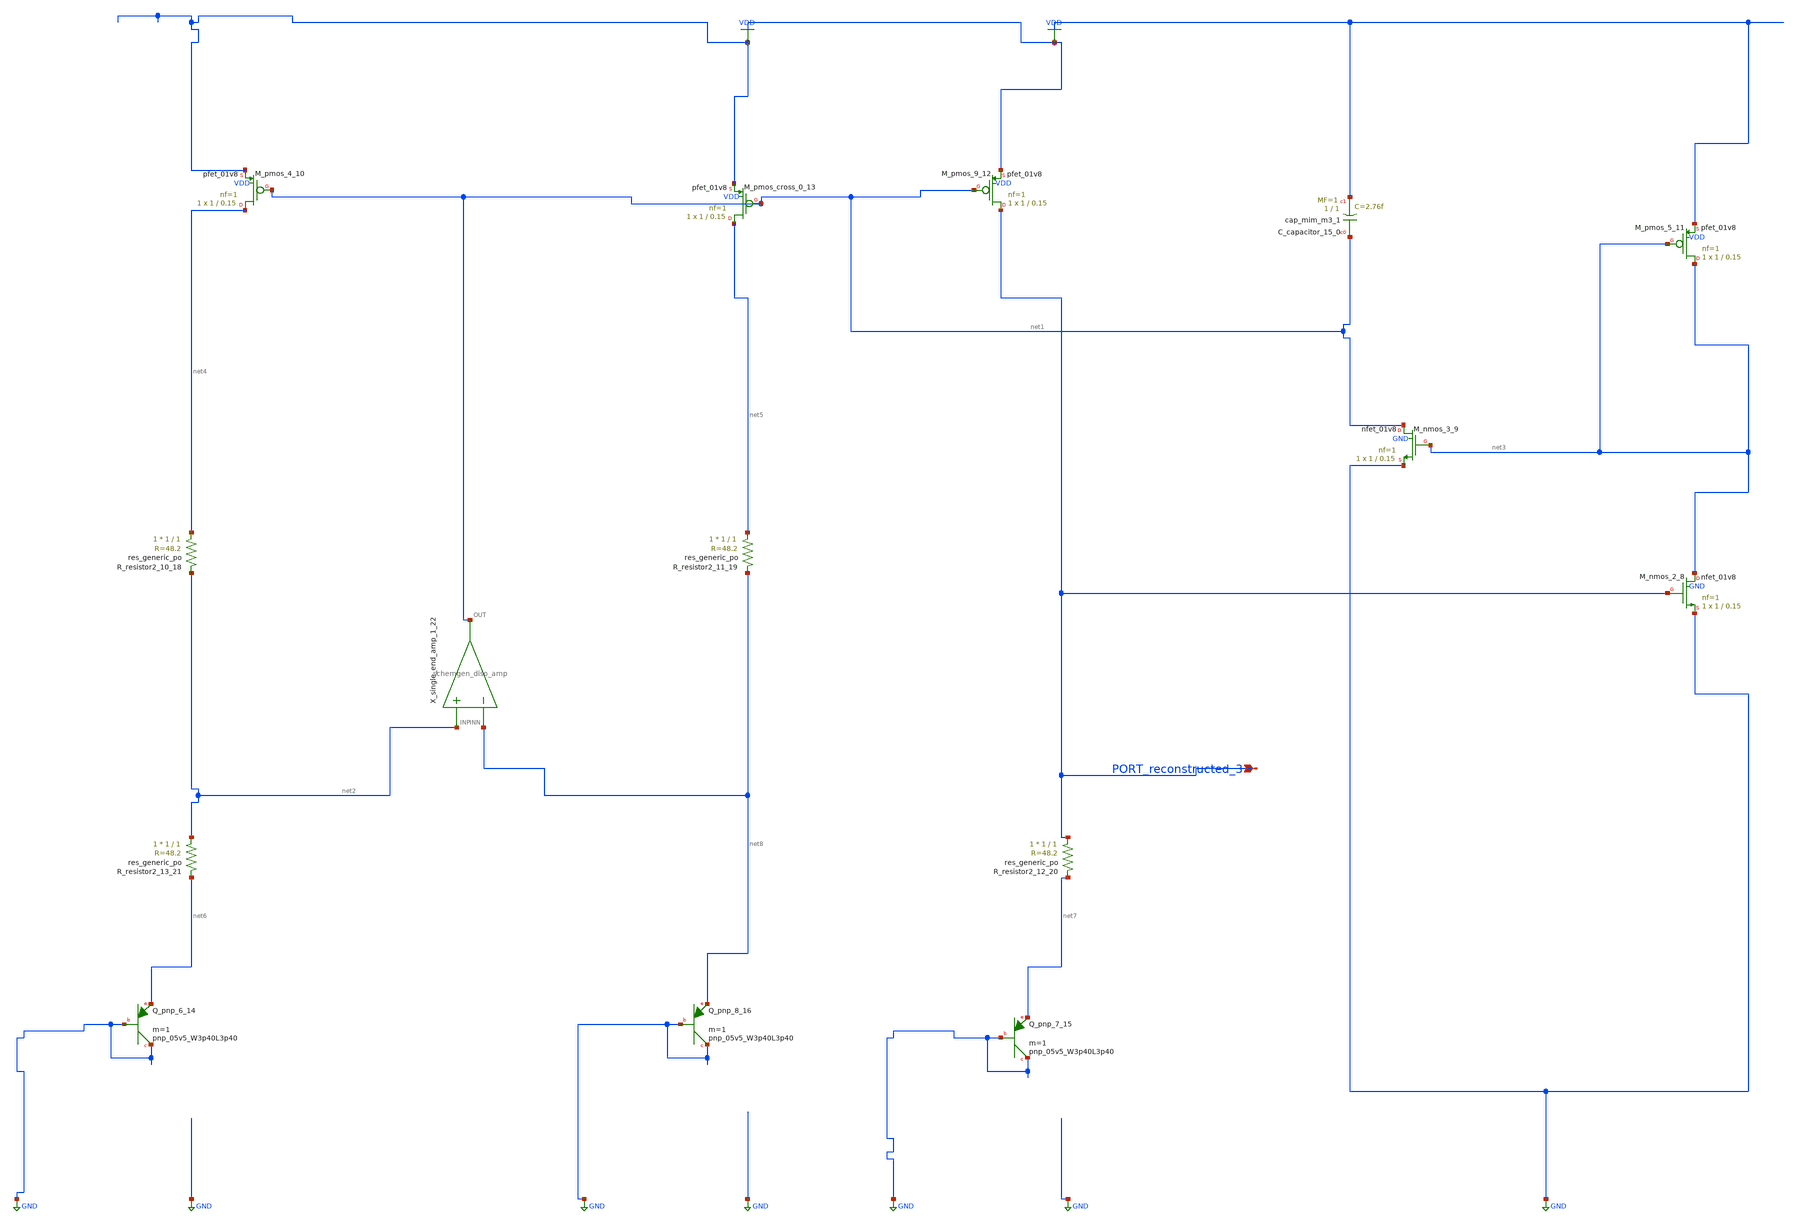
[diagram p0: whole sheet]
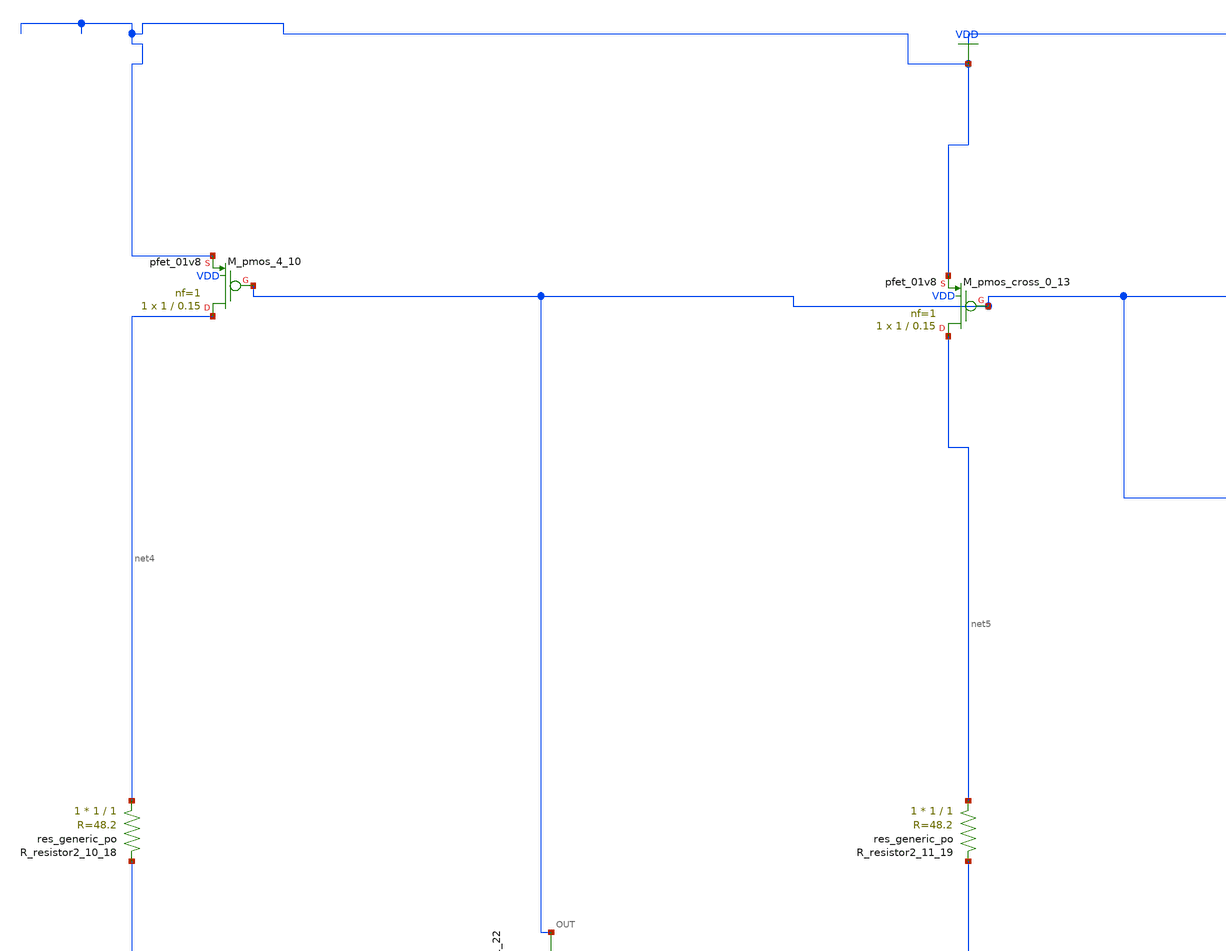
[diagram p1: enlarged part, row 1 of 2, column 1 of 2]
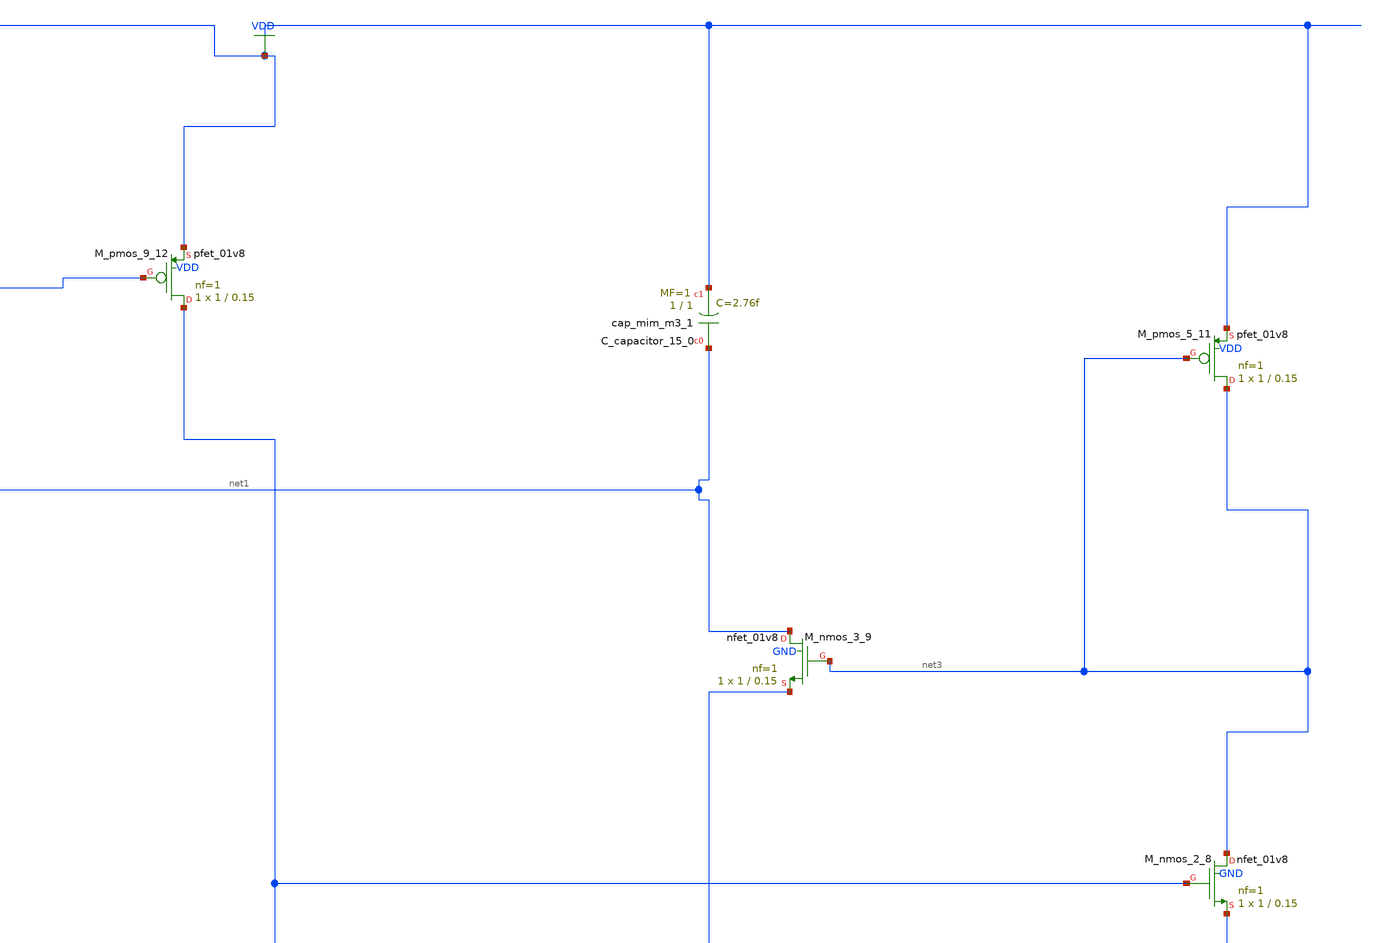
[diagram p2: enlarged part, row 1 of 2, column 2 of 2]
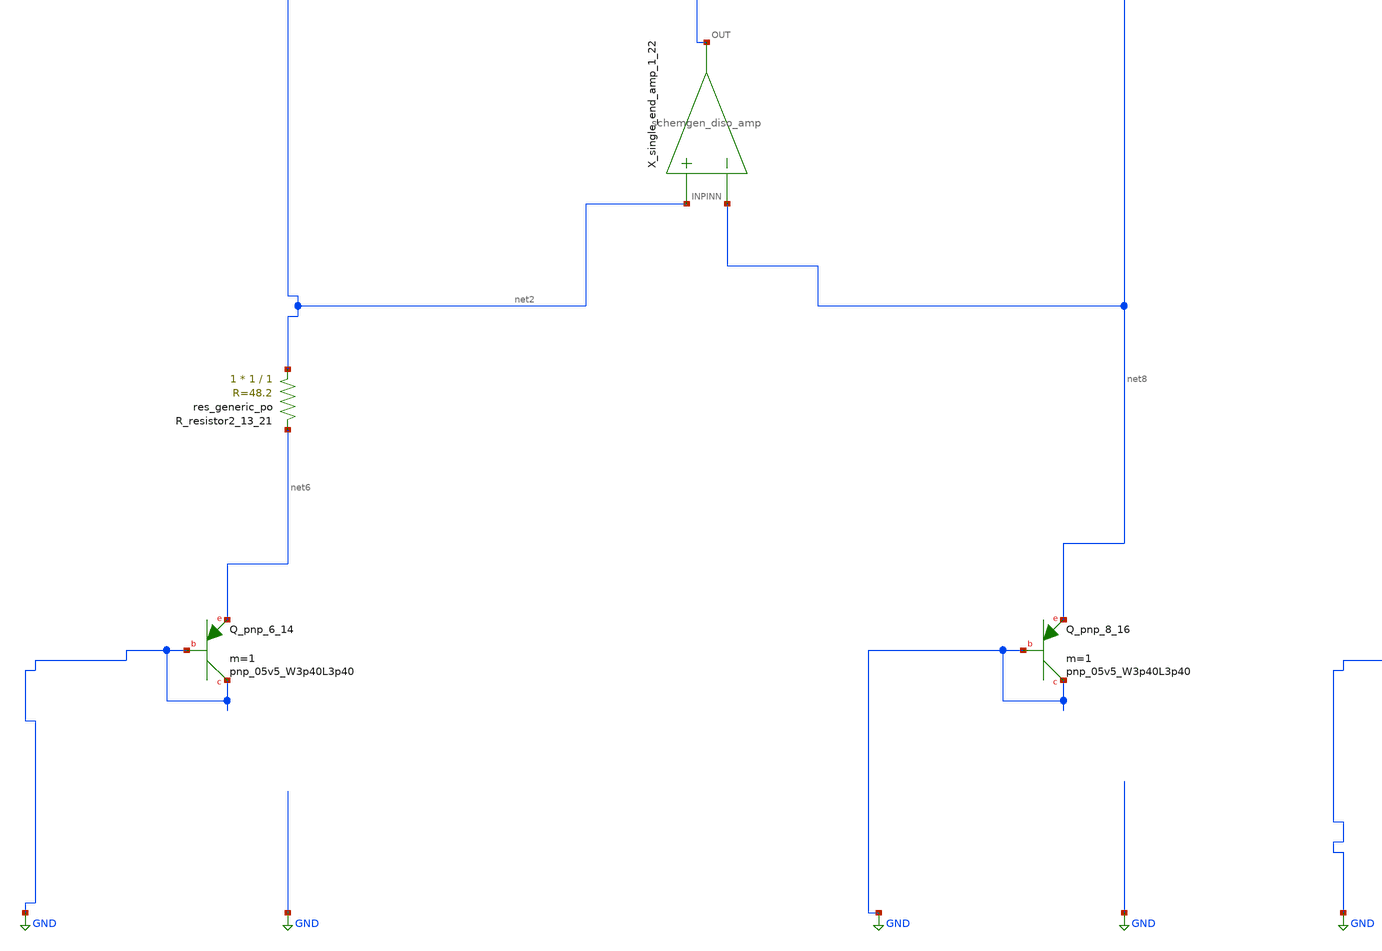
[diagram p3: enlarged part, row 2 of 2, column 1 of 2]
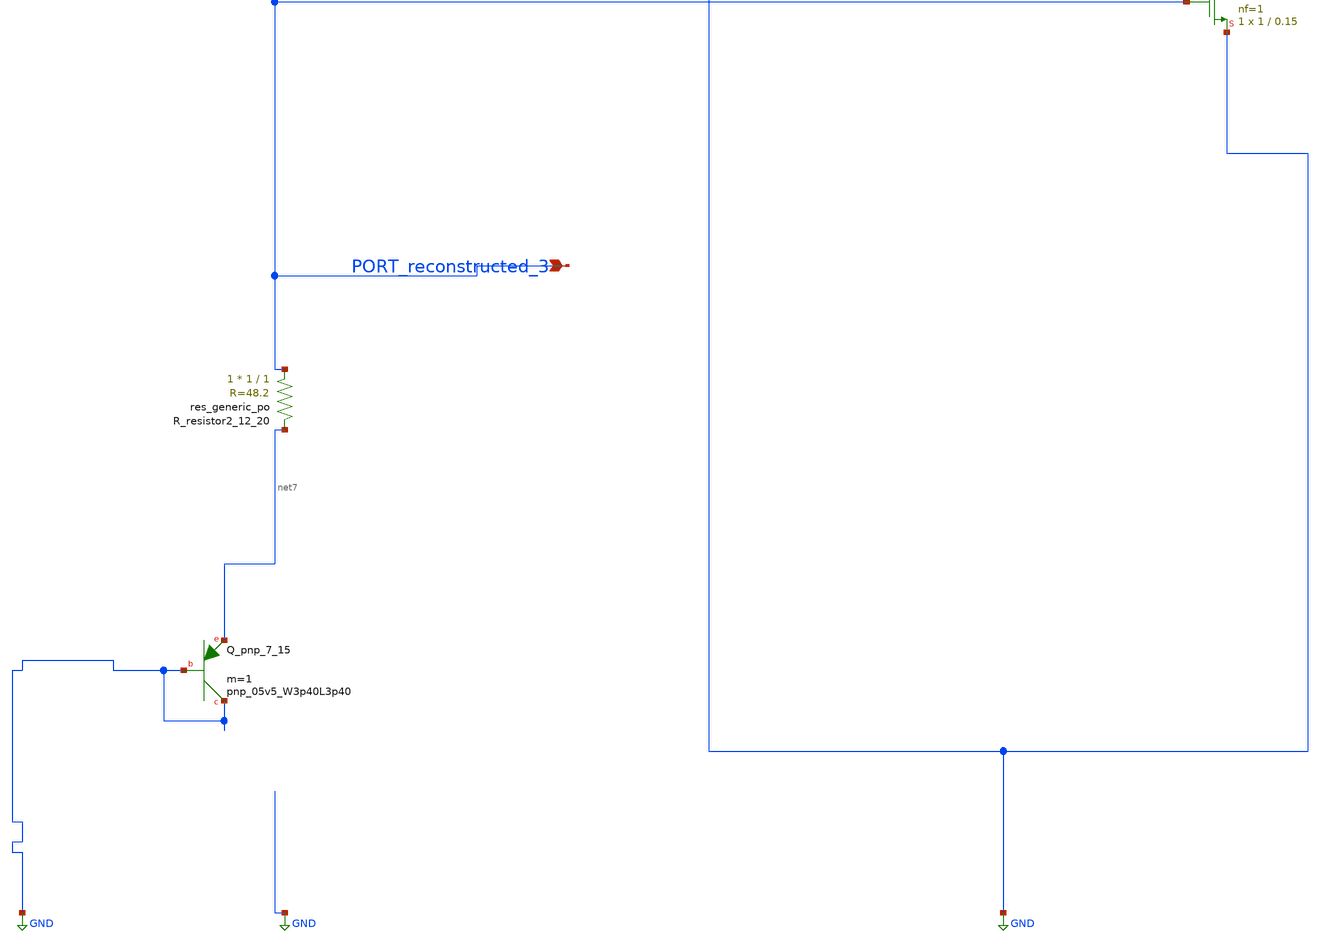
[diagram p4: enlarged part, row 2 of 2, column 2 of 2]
** sch_path: schematics/Image2Net/025.sch
**.subckt 025 PORT_reconstructed_3
*.ipin PORT_reconstructed_3
XC_capacitor_15_0 net1 VDD sky130_fd_pr__cap_mim_m3_1 W=1 L=1 MF=1 m=1
XM_nmos_2_8 net3 PORT_reconstructed_3 GND GND sky130_fd_pr__nfet_01v8 L=0.15 W=1 nf=1 ad='int((1 + 1)/2) * 1 / 1 * 0.29'
+ as='int((1 + 2)/2) * 1 / 1 * 0.29' pd='2*int((1 + 1)/2) * (1 / 1 + 0.29)' ps='2*int((1 + 2)/2) * (1 / 1 + 0.29)'
+ nrd='0.29 / 1 ' nrs='0.29 / 1 ' sa=0 sb=0 sd=0 mult=1 m=1
XM_nmos_3_9 net1 net3 GND GND sky130_fd_pr__nfet_01v8 L=0.15 W=1 nf=1 ad='int((1 + 1)/2) * 1 / 1 * 0.29'
+ as='int((1 + 2)/2) * 1 / 1 * 0.29' pd='2*int((1 + 1)/2) * (1 / 1 + 0.29)' ps='2*int((1 + 2)/2) * (1 / 1 + 0.29)'
+ nrd='0.29 / 1 ' nrs='0.29 / 1 ' sa=0 sb=0 sd=0 mult=1 m=1
XM_pmos_4_10 net4 net1 VDD VDD sky130_fd_pr__pfet_01v8 L=0.15 W=1 nf=1 ad='int((1 + 1)/2) * 1 / 1 * 0.29'
+ as='int((1 + 2)/2) * 1 / 1 * 0.29' pd='2*int((1 + 1)/2) * (1 / 1 + 0.29)' ps='2*int((1 + 2)/2) * (1 / 1 + 0.29)'
+ nrd='0.29 / 1 ' nrs='0.29 / 1 ' sa=0 sb=0 sd=0 mult=1 m=1
XM_pmos_5_11 net3 net3 VDD VDD sky130_fd_pr__pfet_01v8 L=0.15 W=1 nf=1 ad='int((1 + 1)/2) * 1 / 1 * 0.29'
+ as='int((1 + 2)/2) * 1 / 1 * 0.29' pd='2*int((1 + 1)/2) * (1 / 1 + 0.29)' ps='2*int((1 + 2)/2) * (1 / 1 + 0.29)'
+ nrd='0.29 / 1 ' nrs='0.29 / 1 ' sa=0 sb=0 sd=0 mult=1 m=1
XM_pmos_9_12 PORT_reconstructed_3 net1 VDD VDD sky130_fd_pr__pfet_01v8 L=0.15 W=1 nf=1 ad='int((1 + 1)/2) * 1 / 1 * 0.29'
+ as='int((1 + 2)/2) * 1 / 1 * 0.29' pd='2*int((1 + 1)/2) * (1 / 1 + 0.29)' ps='2*int((1 + 2)/2) * (1 / 1 + 0.29)'
+ nrd='0.29 / 1 ' nrs='0.29 / 1 ' sa=0 sb=0 sd=0 mult=1 m=1
XM_pmos_cross_0_13 net5 net1 VDD VDD sky130_fd_pr__pfet_01v8 L=0.15 W=1 nf=1 ad='int((1 + 1)/2) * 1 / 1 * 0.29'
+ as='int((1 + 2)/2) * 1 / 1 * 0.29' pd='2*int((1 + 1)/2) * (1 / 1 + 0.29)' ps='2*int((1 + 2)/2) * (1 / 1 + 0.29)'
+ nrd='0.29 / 1 ' nrs='0.29 / 1 ' sa=0 sb=0 sd=0 mult=1 m=1
XQ_pnp_6_14 GND GND net6 sky130_fd_pr__pnp_05v5_W3p40L3p40 m=1
XQ_pnp_7_15 GND GND net7 sky130_fd_pr__pnp_05v5_W3p40L3p40 m=1
XQ_pnp_8_16 GND GND net8 sky130_fd_pr__pnp_05v5_W3p40L3p40 m=1
XR_resistor2_10_18 net4 net2 sky130_fd_pr__res_generic_po W=1 L=1 m=1
XR_resistor2_11_19 net5 net8 sky130_fd_pr__res_generic_po W=1 L=1 m=1
XR_resistor2_12_20 PORT_reconstructed_3 net7 sky130_fd_pr__res_generic_po W=1 L=1 m=1
XR_resistor2_13_21 net2 net6 sky130_fd_pr__res_generic_po W=1 L=1 m=1
X_single_end_amp_1_22 net2 net8 net1 schemgen_diso_amp
**.ends

* expanding   symbol:  schemgen_diso_amp.sym # of pins=3
** sym_path: symbols/schemgen_diso_amp.sym
.subckt schemgen_diso_amp INP INN OUT
* SchemGen ideal op-amp: Vout = 1e5 * (V(INP) - V(INN))
E1 OUT 0 INP INN 1e5
.ends schemgen_diso_amp
.GLOBAL GND
.GLOBAL VDD
.end
